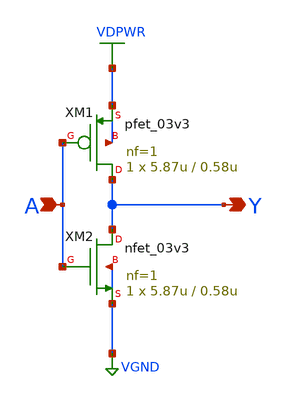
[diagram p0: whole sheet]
** sch_path: xschem/skullfet_inverter.sch
**.subckt skullfet_inverter A Y
*.ipin A
*.opin Y
XM1 Y A VDPWR VDPWR pfet_03v3 L=0.58u W=5.87u nf=1 ad='int((nf+1)/2) * W/nf * 0.18u' as='int((nf+2)/2) * W/nf * 0.18u'
+ pd='2*int((nf+1)/2) * (W/nf + 0.18u)' ps='2*int((nf+2)/2) * (W/nf + 0.18u)' nrd='0.18u / W' nrs='0.18u / W'
+ sa=0 sb=0 sd=0 m=1
XM2 Y A VGND VGND nfet_03v3 L=0.58u W=5.87u nf=1 ad='int((nf+1)/2) * W/nf * 0.18u' as='int((nf+2)/2) * W/nf * 0.18u'
+ pd='2*int((nf+1)/2) * (W/nf + 0.18u)' ps='2*int((nf+2)/2) * (W/nf + 0.18u)' nrd='0.18u / W' nrs='0.18u / W'
+ sa=0 sb=0 sd=0 m=1
**.ends
.GLOBAL VGND
.GLOBAL VDPWR
.end
